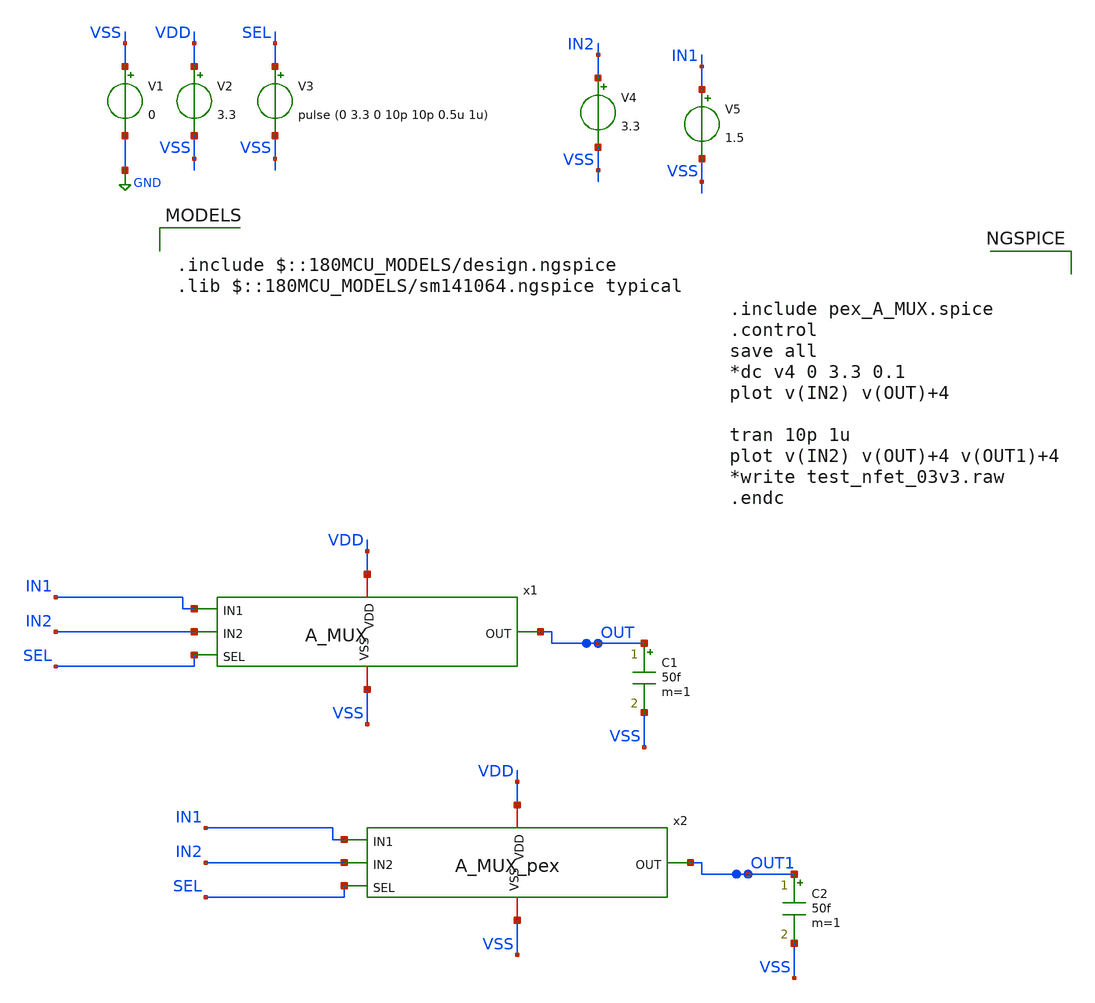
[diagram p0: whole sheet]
** sch_path: Clock_Generator_PAKISTAN_02/Schematics/A_MUX_TB.sch
**.subckt A_MUX_TB
C1 OUT VSS 50f m=1
V1 VSS GND 0
V2 VDD VSS 3.3
V3 SEL VSS pulse (0 3.3 0 10p 10p 0.5u 1u)
x1 VDD VSS IN1 IN2 SEL OUT A_MUX
V4 IN2 VSS 3.3
V5 IN1 VSS 1.5
C2 OUT1 VSS 50f m=1
x2 VDD VSS IN1 IN2 SEL OUT1 A_MUX_pex
**** begin user architecture code

.include $::180MCU_MODELS/design.ngspice
.lib $::180MCU_MODELS/sm141064.ngspice typical




.include pex_A_MUX.spice
.control
save all
*dc v4 0 3.3 0.1
plot v(IN2) v(OUT)+4

tran 10p 1u
plot v(IN2) v(OUT)+4 v(OUT1)+4
*write test_nfet_03v3.raw
.endc


**** end user architecture code
**.ends
.GLOBAL GND
.end
